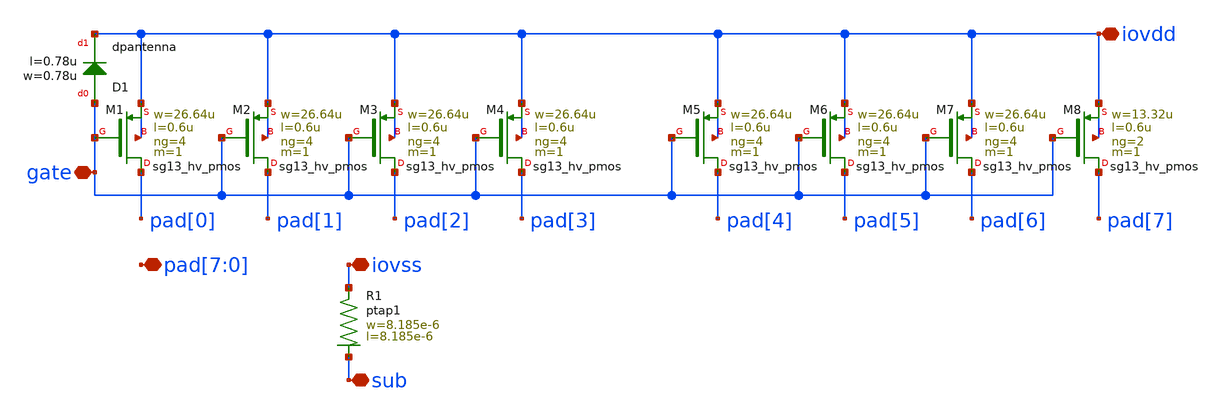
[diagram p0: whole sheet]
** sch_path: MSPHY6034-main/dependencies/unic_cass_2025_team04_padring/xschem/openpdk-libraries/ihp-sg13g2/sg13g2_io/xschem/sg13g2_Clamp_P15N15D.sch
**.subckt sg13g2_Clamp_P15N15D iovss gate iovdd
*+ pad[7],pad[6],pad[5],pad[4],pad[3],pad[2],pad[1],pad[0] sub
*.iopin iovss
*.iopin gate
*.iopin iovdd
*.iopin pad[7],pad[6],pad[5],pad[4],pad[3],pad[2],pad[1],pad[0]
*.iopin sub
XR1 iovss sub ptap1 R=9.826 w=8.185e-6 l=8.185e-6
XM1 pad[0] gate iovdd iovdd sg13_hv_pmos w=26.64u l=0.6u ng=4 m=1 mm_ok=1
XD1 gate iovdd dpantenna l=0.78u w=0.78u
XM2 pad[1] gate iovdd iovdd sg13_hv_pmos w=26.64u l=0.6u ng=4 m=1 mm_ok=1
XM3 pad[2] gate iovdd iovdd sg13_hv_pmos w=26.64u l=0.6u ng=4 m=1 mm_ok=1
XM4 pad[3] gate iovdd iovdd sg13_hv_pmos w=26.64u l=0.6u ng=4 m=1 mm_ok=1
XM5 pad[4] gate iovdd iovdd sg13_hv_pmos w=26.64u l=0.6u ng=4 m=1 mm_ok=1
XM6 pad[5] gate iovdd iovdd sg13_hv_pmos w=26.64u l=0.6u ng=4 m=1 mm_ok=1
XM7 pad[6] gate iovdd iovdd sg13_hv_pmos w=26.64u l=0.6u ng=4 m=1 mm_ok=1
XM8 pad[7] gate iovdd iovdd sg13_hv_pmos w=13.32u l=0.6u ng=2 m=1 mm_ok=1
**.ends
.end
